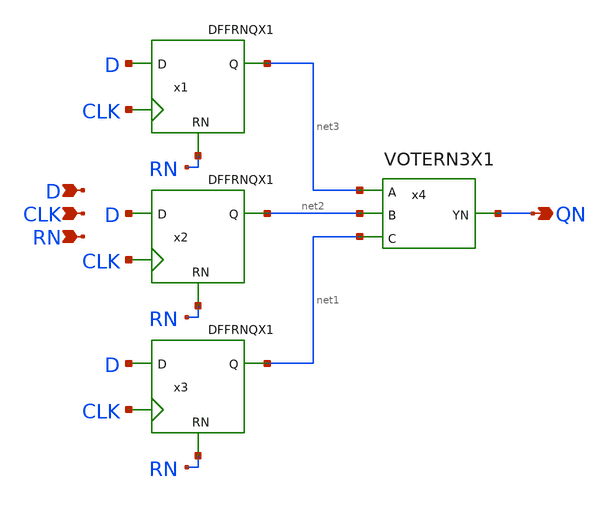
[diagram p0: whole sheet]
** sch_path: archives/lib/xschem/TMRDFFRNQNX1.sch
**.subckt TMRDFFRNQNX1 QN D CLK RN
*.opin QN
*.ipin D
*.ipin CLK
*.ipin RN
x1 net3 D CLK RN VDD VSS DFFRNQX1
x2 net2 D CLK RN VDD VSS DFFRNQX1
x3 net1 D CLK RN VDD VSS DFFRNQX1
x4 net3 net2 net1 QN VDD VSS VOTERN3X1
**.ends
.end
